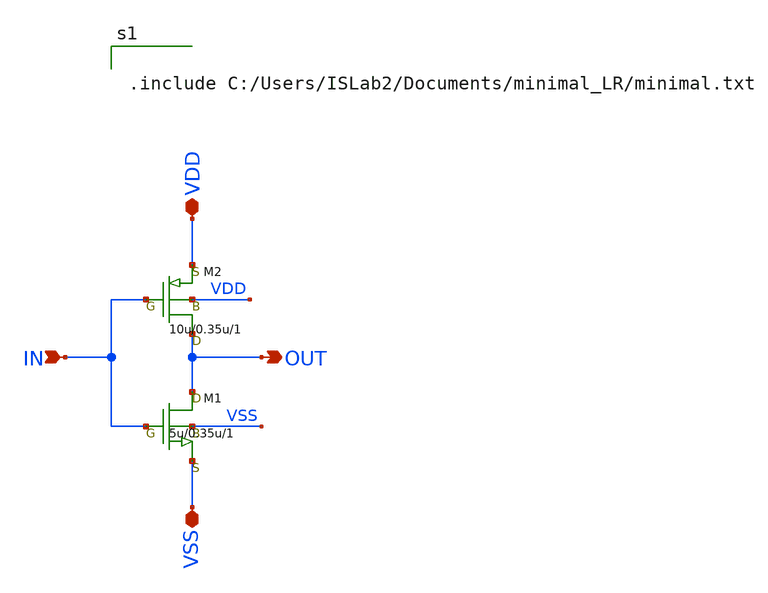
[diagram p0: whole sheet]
** sch_path: INV.sch
**.subckt INV OUT IN VDD VSS
*.opin OUT
*.ipin IN
*.iopin VDD
*.iopin VSS
M2 OUT IN VDD VDD pch w=10u l=0.35u as=0 ps=0 ad=0 pd=0 m=1
M1 OUT IN VSS VSS nch w=5u l=0.35u as=0 ps=0 ad=0 pd=0 m=1
**** begin user architecture code


.include C:/Users/ISLab2/Documents/minimal_LR/minimal.txt

**** end user architecture code
**.ends
.end
